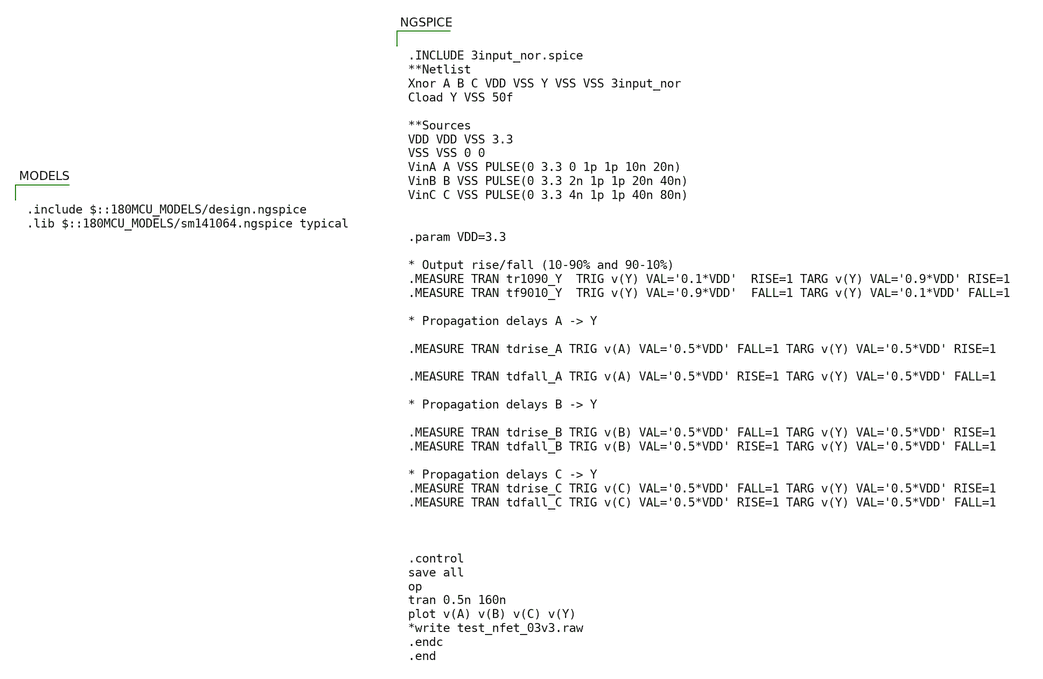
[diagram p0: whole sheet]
** sch_path: designs/libs/core_digital/gf180mcu_osu_sc_gp9t3v3/cells/nor3/TB_3input_nor.sch
**.subckt TB_3input_nor
**** begin user architecture code


.INCLUDE 3input_nor.spice
**Netlist
Xnor A B C VDD VSS Y VSS VSS 3input_nor
Cload Y VSS 50f

**Sources
VDD VDD VSS 3.3
VSS VSS 0 0
VinA A VSS PULSE(0 3.3 0 1p 1p 10n 20n)
VinB B VSS PULSE(0 3.3 2n 1p 1p 20n 40n)
VinC C VSS PULSE(0 3.3 4n 1p 1p 40n 80n)


.param VDD=3.3

* Output rise/fall (10-90% and 90-10%)
.MEASURE TRAN tr1090_Y  TRIG v(Y) VAL='0.1*VDD'  RISE=1 TARG v(Y) VAL='0.9*VDD' RISE=1
.MEASURE TRAN tf9010_Y  TRIG v(Y) VAL='0.9*VDD'  FALL=1 TARG v(Y) VAL='0.1*VDD' FALL=1

* Propagation delays A -> Y

.MEASURE TRAN tdrise_A TRIG v(A) VAL='0.5*VDD' FALL=1 TARG v(Y) VAL='0.5*VDD' RISE=1

.MEASURE TRAN tdfall_A TRIG v(A) VAL='0.5*VDD' RISE=1 TARG v(Y) VAL='0.5*VDD' FALL=1

* Propagation delays B -> Y

.MEASURE TRAN tdrise_B TRIG v(B) VAL='0.5*VDD' FALL=1 TARG v(Y) VAL='0.5*VDD' RISE=1
.MEASURE TRAN tdfall_B TRIG v(B) VAL='0.5*VDD' RISE=1 TARG v(Y) VAL='0.5*VDD' FALL=1

* Propagation delays C -> Y
.MEASURE TRAN tdrise_C TRIG v(C) VAL='0.5*VDD' FALL=1 TARG v(Y) VAL='0.5*VDD' RISE=1
.MEASURE TRAN tdfall_C TRIG v(C) VAL='0.5*VDD' RISE=1 TARG v(Y) VAL='0.5*VDD' FALL=1



.control
save all
op
tran 0.5n 160n
plot v(A) v(B) v(C) v(Y)
*write test_nfet_03v3.raw
.endc
.end



.include $::180MCU_MODELS/design.ngspice
.lib $::180MCU_MODELS/sm141064.ngspice typical

**** end user architecture code
**.ends
.end
